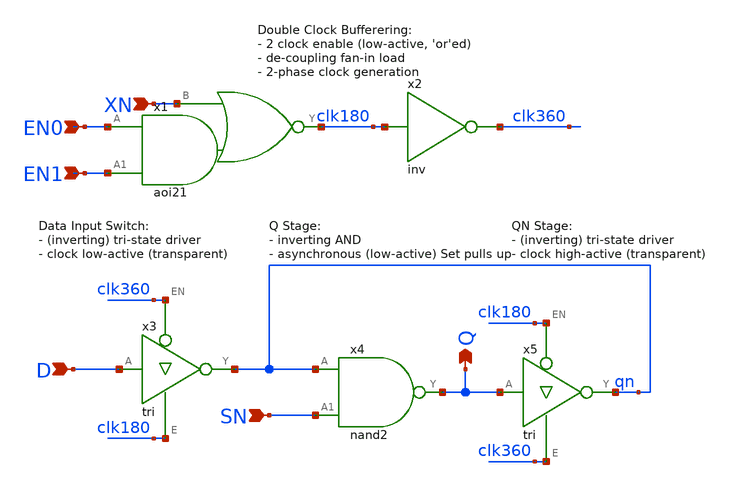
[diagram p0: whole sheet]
** sch_path: Sources/crafted/LATEESN.sch
**.subckt LATEESN XN D Q EN0 EN1 SN
*.ipin XN
*.ipin D
*.opin Q
*.ipin EN0
*.ipin EN1
*.ipin SN
x2 clk180 clk360 VDD GND inv Wmin=1.5u Lmin=1u g=2 m=1
x3 D clk360 clk180 qn VDD GND tri Wmin=1.5u Lmin=1u g=2 m=1
x5 Q clk180 clk360 qn VDD GND tri Wmin=1.5u Lmin=1u g=2 m=1
x1 EN0 EN1 clk180 XN VDD GND aoi21 Wmin=1.5u Lmin=1u g=2 m=1
x4 Q qn SN VDD GND nand2 Wmin=1.5u Lmin=1u g=2 m=1
**.ends
.end
